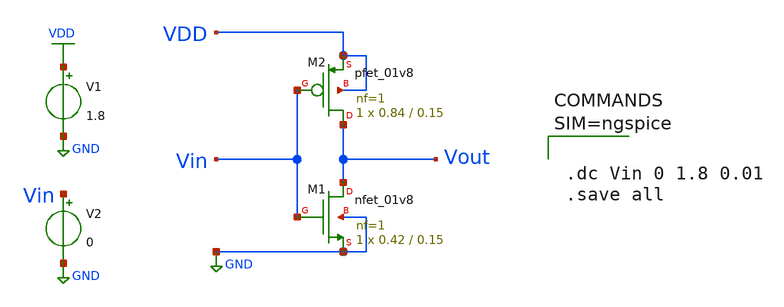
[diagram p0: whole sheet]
** sch_path: mySAR_SKY130/xschem/test/untitled.sch
**.subckt untitled
XM1 Vout Vin GND GND sky130_fd_pr__nfet_01v8 L=0.15 W=0.42 nf=1 ad='int((nf+1)/2) * W/nf * 0.29' as='int((nf+2)/2) * W/nf * 0.29'
+ pd='2*int((nf+1)/2) * (W/nf + 0.29)' ps='2*int((nf+2)/2) * (W/nf + 0.29)' nrd='0.29 / W' nrs='0.29 / W'
+ sa=0 sb=0 sd=0 mult=1 m=1
XM2 Vout Vin VDD VDD sky130_fd_pr__pfet_01v8 L=0.15 W=0.84 nf=1 ad='int((nf+1)/2) * W/nf * 0.29' as='int((nf+2)/2) * W/nf * 0.29'
+ pd='2*int((nf+1)/2) * (W/nf + 0.29)' ps='2*int((nf+2)/2) * (W/nf + 0.29)' nrd='0.29 / W' nrs='0.29 / W'
+ sa=0 sb=0 sd=0 mult=1 m=1
V1 VDD GND 1.8
V2 Vin GND 0
**** begin user architecture code



.dc Vin 0 1.8 0.01
.save all



**** end user architecture code
**.ends
.GLOBAL GND
.GLOBAL VDD
.end
